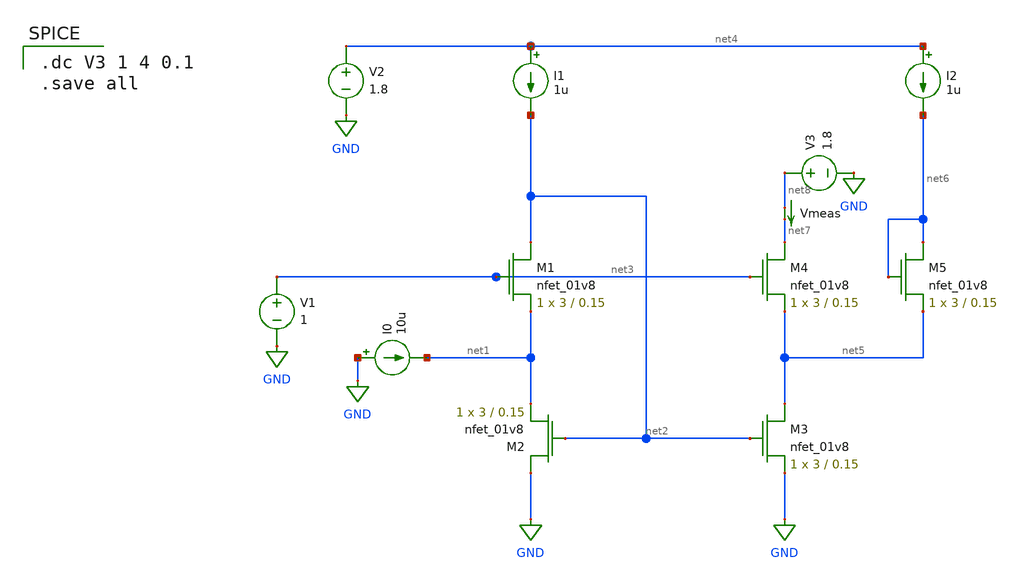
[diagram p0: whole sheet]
** sch_path: FVF_CCM_test.sch
**.subckt FVF_CCM_test
XM1 net2 net3 net1 GND sky130_fd_pr__nfet_01v8 L=0.15 W=3 nf=1 ad='int((nf+1)/2) * W/nf * 0.29' as='int((nf+2)/2) * W/nf * 0.29'
+ pd='2*int((nf+1)/2) * (W/nf + 0.29)' ps='2*int((nf+2)/2) * (W/nf + 0.29)' nrd='0.29 / W' nrs='0.29 / W'
+ sa=0 sb=0 sd=0 mult=1 m=1
XM2 GND net2 net1 GND sky130_fd_pr__nfet_01v8 L=0.15 W=3 nf=1 ad='int((nf+1)/2) * W/nf * 0.29' as='int((nf+2)/2) * W/nf * 0.29'
+ pd='2*int((nf+1)/2) * (W/nf + 0.29)' ps='2*int((nf+2)/2) * (W/nf + 0.29)' nrd='0.29 / W' nrs='0.29 / W'
+ sa=0 sb=0 sd=0 mult=1 m=1
I0 GND net1 10u
V1 net3 GND 1
I1 net4 net2 1u
V2 net4 GND 1.8
XM3 net5 net2 GND GND sky130_fd_pr__nfet_01v8 L=0.15 W=3 nf=1 ad='int((nf+1)/2) * W/nf * 0.29' as='int((nf+2)/2) * W/nf * 0.29'
+ pd='2*int((nf+1)/2) * (W/nf + 0.29)' ps='2*int((nf+2)/2) * (W/nf + 0.29)' nrd='0.29 / W' nrs='0.29 / W'
+ sa=0 sb=0 sd=0 mult=1 m=1
XM4 net7 net3 net5 GND sky130_fd_pr__nfet_01v8 L=0.15 W=3 nf=1 ad='int((nf+1)/2) * W/nf * 0.29' as='int((nf+2)/2) * W/nf * 0.29'
+ pd='2*int((nf+1)/2) * (W/nf + 0.29)' ps='2*int((nf+2)/2) * (W/nf + 0.29)' nrd='0.29 / W' nrs='0.29 / W'
+ sa=0 sb=0 sd=0 mult=1 m=1
XM5 net6 net6 net5 GND sky130_fd_pr__nfet_01v8 L=0.15 W=3 nf=1 ad='int((nf+1)/2) * W/nf * 0.29' as='int((nf+2)/2) * W/nf * 0.29'
+ pd='2*int((nf+1)/2) * (W/nf + 0.29)' ps='2*int((nf+2)/2) * (W/nf + 0.29)' nrd='0.29 / W' nrs='0.29 / W'
+ sa=0 sb=0 sd=0 mult=1 m=1
I2 net4 net6 1u
V3 net8 GND 1.8
Vmeas net8 net7 0
.save i(vmeas)
**** begin user architecture code

.lib $::SKYWATER_MODELS/sky130.lib.spice tt


.dc V3 1 4 0.1
.save all

**** end user architecture code
**.ends
.GLOBAL GND
.end
